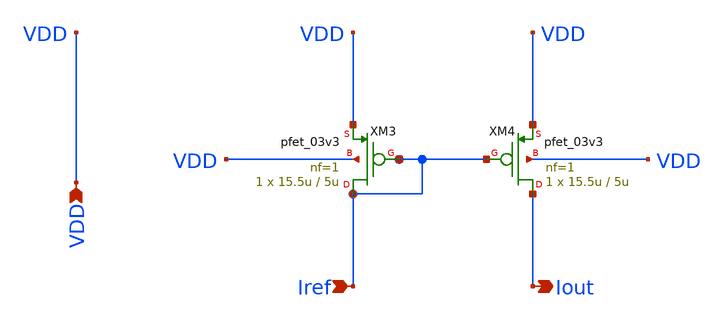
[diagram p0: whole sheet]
** sch_path: designs/libs/core_current-mirror/pmos_current_mirror/pmos_current_mirror.sch
**.subckt pmos_current_mirror VDD Iref Iout
*.ipin VDD
*.ipin Iref
*.opin Iout
XM3 Iref Iref VDD VDD pfet_03v3 L=5u W=15.5u nf=1 ad='int((nf+1)/2) * W/nf * 0.18u' as='int((nf+2)/2) * W/nf * 0.18u'
+ pd='2*int((nf+1)/2) * (W/nf + 0.18u)' ps='2*int((nf+2)/2) * (W/nf + 0.18u)' nrd='0.18u / W' nrs='0.18u / W'
+ sa=0 sb=0 sd=0 m=1
XM4 Iout Iref VDD VDD pfet_03v3 L=5u W=15.5u nf=1 ad='int((nf+1)/2) * W/nf * 0.18u' as='int((nf+2)/2) * W/nf * 0.18u'
+ pd='2*int((nf+1)/2) * (W/nf + 0.18u)' ps='2*int((nf+2)/2) * (W/nf + 0.18u)' nrd='0.18u / W' nrs='0.18u / W'
+ sa=0 sb=0 sd=0 m=1
**.ends
.end
